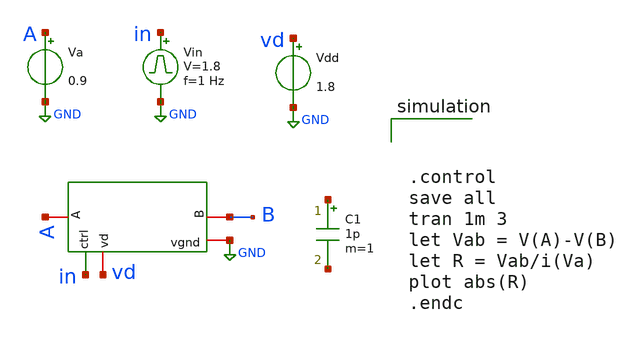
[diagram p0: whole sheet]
** sch_path: xschem/tg-tb.sch
**.subckt tg-tb
Vdd vd GND 1.8
Vin in GND pulse 0 1.8 '0.495/ 1 ' '0.01/1 ' '0.01/1 ' '0.49/1 ' '1/1 '
x1 vd in GND A B tg
Va A GND 0.9
C1 net1 net2 1p m=1
**** begin user architecture code

** opencircuitdesign pdks install
.lib $::SKYWATER_MODELS/sky130.lib.spice tt





.control
save all
tran 1m 3
let Vab = V(A)-V(B)
let R = Vab/i(Va)
plot abs(R)
.endc


**** end user architecture code
**.ends

* expanding   symbol:  /foss/designs/tg.sym # of pins=5
** sym_path: xschem/tg.sym
** sch_path: xschem/tg.sch
.subckt tg vd ctrl vgnd A B
*.iopin B
*.iopin A
*.iopin vgnd
*.iopin vd
*.ipin ctrl
x1 vd ctrl nctrl vgnd inverter
XM1 A ctrl B vgnd sky130_fd_pr__nfet_01v8 L=0.15 W=10 nf=1 ad='int((nf+1)/2) * W/nf * 0.29' as='int((nf+2)/2) * W/nf * 0.29'
+ pd='2*int((nf+1)/2) * (W/nf + 0.29)' ps='2*int((nf+2)/2) * (W/nf + 0.29)' nrd='0.29 / W' nrs='0.29 / W'
+ sa=0 sb=0 sd=0 mult=1 m=1
XM2 A nctrl B vd sky130_fd_pr__pfet_01v8 L=0.15 W=30 nf=1 ad='int((nf+1)/2) * W/nf * 0.29' as='int((nf+2)/2) * W/nf * 0.29'
+ pd='2*int((nf+1)/2) * (W/nf + 0.29)' ps='2*int((nf+2)/2) * (W/nf + 0.29)' nrd='0.29 / W' nrs='0.29 / W'
+ sa=0 sb=0 sd=0 mult=1 m=1
.ends


* expanding   symbol:  /foss/designs/inverter/xschem_files/inverter.sym # of pins=4
** sym_path: /foss/designs/inverter/xschem_files/inverter.sym
** sch_path: /foss/designs/inverter/xschem_files/inverter.sch
.subckt inverter vd in out gnd
*.ipin in
*.opin out
*.iopin vd
*.iopin gnd
XN0 out in gnd gnd sky130_fd_pr__nfet_01v8 L=0.15 W=1 nf=1 ad='int((nf+1)/2) * W/nf * 0.29' as='int((nf+2)/2) * W/nf * 0.29'
+ pd='2*int((nf+1)/2) * (W/nf + 0.29)' ps='2*int((nf+2)/2) * (W/nf + 0.29)' nrd='0.29 / W' nrs='0.29 / W'
+ sa=0 sb=0 sd=0 mult=1 m=1
XP0 out in vd vd sky130_fd_pr__pfet_01v8 L=0.15 W=3 nf=1 ad='int((nf+1)/2) * W/nf * 0.29' as='int((nf+2)/2) * W/nf * 0.29'
+ pd='2*int((nf+1)/2) * (W/nf + 0.29)' ps='2*int((nf+2)/2) * (W/nf + 0.29)' nrd='0.29 / W' nrs='0.29 / W'
+ sa=0 sb=0 sd=0 mult=1 m=1
.ends

.GLOBAL GND
.end
